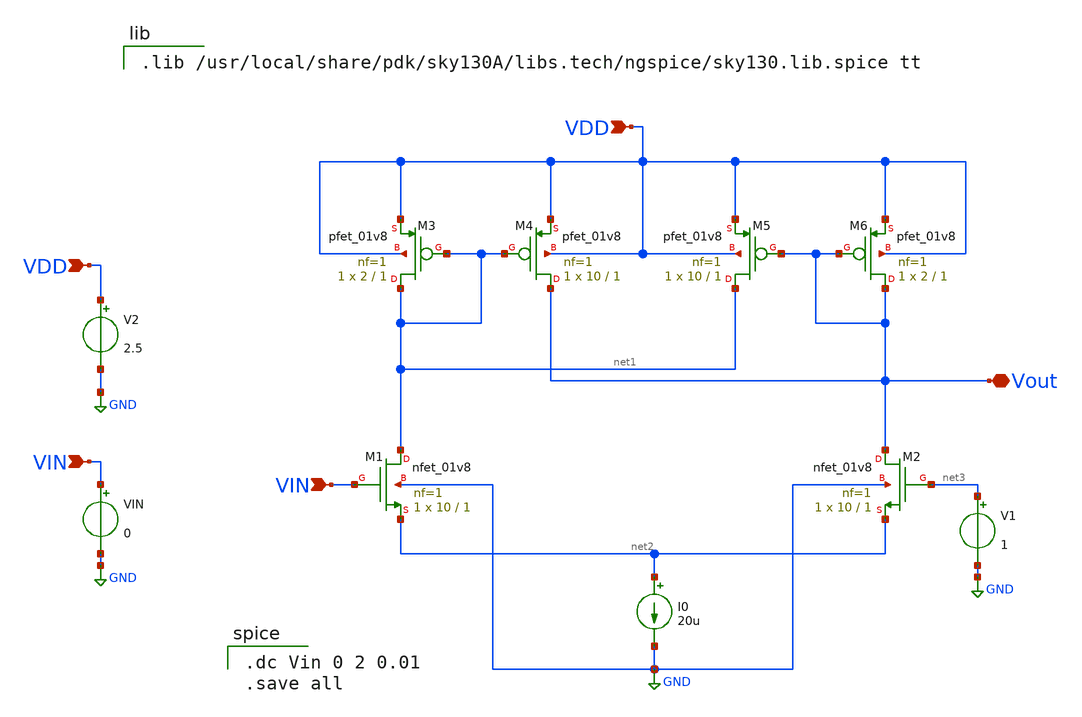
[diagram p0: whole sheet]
** sch_path: xschem/Comparador.sch
**.subckt Comparador VDD VDD Vout VIN VIN
*.ipin VDD
*.ipin VDD
*.iopin Vout
*.ipin VIN
*.ipin VIN
XM1 net1 VIN net2 GND sky130_fd_pr__nfet_01v8 L=1 W=10 nf=1 ad='int((nf+1)/2) * W/nf * 0.29' as='int((nf+2)/2) * W/nf * 0.29'
+ pd='2*int((nf+1)/2) * (W/nf + 0.29)' ps='2*int((nf+2)/2) * (W/nf + 0.29)' nrd='0.29 / W' nrs='0.29 / W'
+ sa=0 sb=0 sd=0 mult=1 m=1
XM2 Vout net3 net2 GND sky130_fd_pr__nfet_01v8 L=1 W=10 nf=1 ad='int((nf+1)/2) * W/nf * 0.29' as='int((nf+2)/2) * W/nf * 0.29'
+ pd='2*int((nf+1)/2) * (W/nf + 0.29)' ps='2*int((nf+2)/2) * (W/nf + 0.29)' nrd='0.29 / W' nrs='0.29 / W'
+ sa=0 sb=0 sd=0 mult=1 m=1
XM3 net1 net1 VDD VDD sky130_fd_pr__pfet_01v8 L=1 W=2 nf=1 ad='int((nf+1)/2) * W/nf * 0.29' as='int((nf+2)/2) * W/nf * 0.29'
+ pd='2*int((nf+1)/2) * (W/nf + 0.29)' ps='2*int((nf+2)/2) * (W/nf + 0.29)' nrd='0.29 / W' nrs='0.29 / W'
+ sa=0 sb=0 sd=0 mult=1 m=1
XM4 Vout net1 VDD VDD sky130_fd_pr__pfet_01v8 L=1 W=10 nf=1 ad='int((nf+1)/2) * W/nf * 0.29' as='int((nf+2)/2) * W/nf * 0.29'
+ pd='2*int((nf+1)/2) * (W/nf + 0.29)' ps='2*int((nf+2)/2) * (W/nf + 0.29)' nrd='0.29 / W' nrs='0.29 / W'
+ sa=0 sb=0 sd=0 mult=1 m=1
XM5 net1 Vout VDD VDD sky130_fd_pr__pfet_01v8 L=1 W=10 nf=1 ad='int((nf+1)/2) * W/nf * 0.29' as='int((nf+2)/2) * W/nf * 0.29'
+ pd='2*int((nf+1)/2) * (W/nf + 0.29)' ps='2*int((nf+2)/2) * (W/nf + 0.29)' nrd='0.29 / W' nrs='0.29 / W'
+ sa=0 sb=0 sd=0 mult=1 m=1
XM6 Vout Vout VDD VDD sky130_fd_pr__pfet_01v8 L=1 W=2 nf=1 ad='int((nf+1)/2) * W/nf * 0.29' as='int((nf+2)/2) * W/nf * 0.29'
+ pd='2*int((nf+1)/2) * (W/nf + 0.29)' ps='2*int((nf+2)/2) * (W/nf + 0.29)' nrd='0.29 / W' nrs='0.29 / W'
+ sa=0 sb=0 sd=0 mult=1 m=1
V1 net3 GND 1
I0 net2 GND 20u
V2 VDD GND 2.5
VIN VIN GND 0
**** begin user architecture code

.dc Vin 0 2 0.01
.save all


.lib /usr/local/share/pdk/sky130A/libs.tech/ngspice/sky130.lib.spice tt

**** end user architecture code
**.ends
.GLOBAL GND
.end
